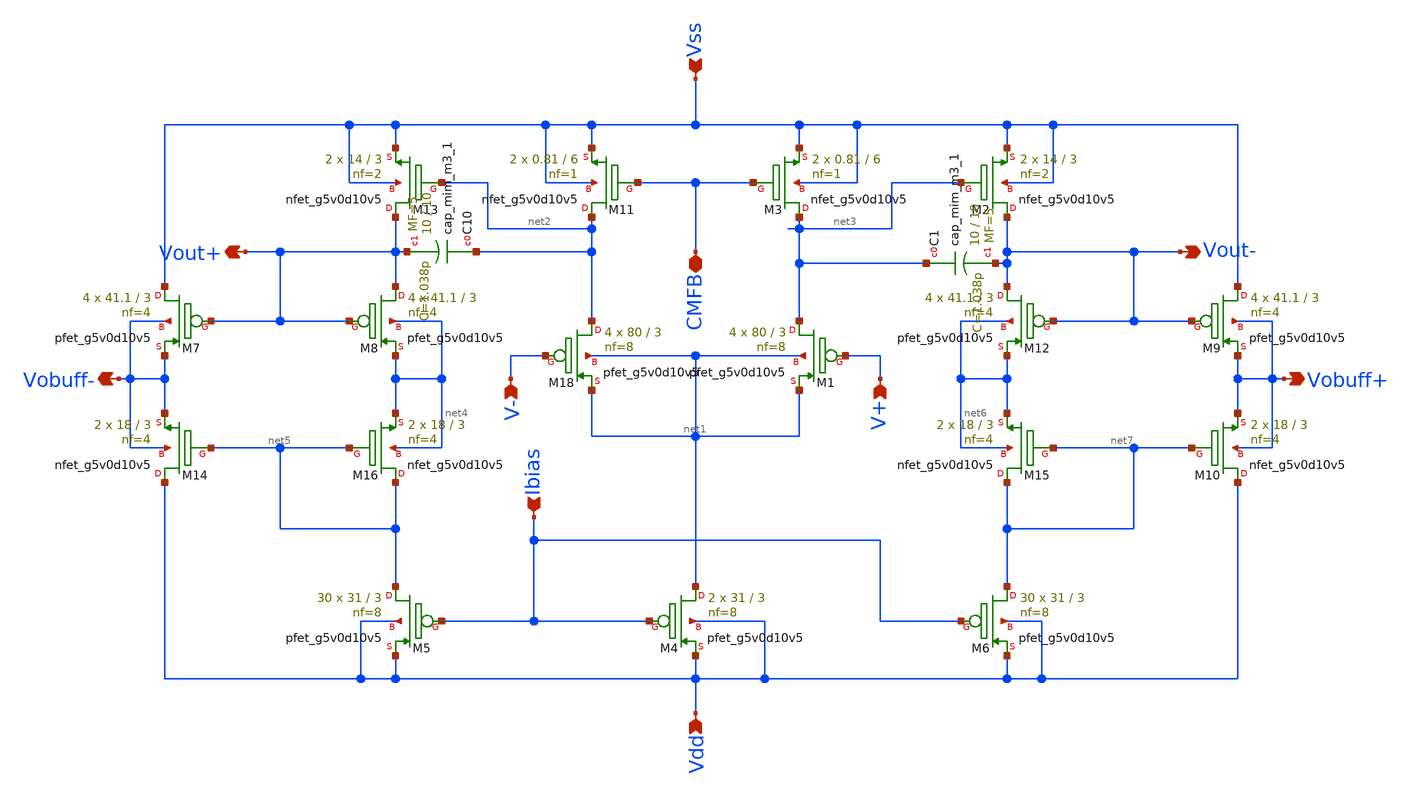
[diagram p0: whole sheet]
** sch_path: xschem/Diff_OP_AMP.sch
**.subckt Diff_OP_AMP Vout+ Vdd Vss V+ V- Vout- Ibias Vobuff- Vobuff+ CMFB
*.opin Vout+
*.ipin Vdd
*.ipin Vss
*.ipin V+
*.ipin V-
*.opin Vout-
*.ipin Ibias
*.opin Vobuff-
*.opin Vobuff+
*.iopin CMFB
XM4 net1 Ibias Vdd Vdd sky130_fd_pr__pfet_g5v0d10v5 L=3 W=31 nf=8 ad='int((8 + 1)/2) * 31 / 8 * 0.29'
+ as='int((8 + 2)/2) * 31 / 8 * 0.29' pd='2*int((8 + 1)/2) * (31 / 8 + 0.29)' ps='2*int((8 + 2)/2) * (31 / 8 + 0.29)'
+ nrd='0.29 / 31 ' nrs='0.29 / 31 ' sa=0 sb=0 sd=0 mult=2 m=2
XM18 net2 V- net1 net1 sky130_fd_pr__pfet_g5v0d10v5 L=3 W=80 nf=8 ad='int((8 + 1)/2) * 80 / 8 * 0.29'
+ as='int((8 + 2)/2) * 80 / 8 * 0.29' pd='2*int((8 + 1)/2) * (80 / 8 + 0.29)' ps='2*int((8 + 2)/2) * (80 / 8 + 0.29)'
+ nrd='0.29 / 80 ' nrs='0.29 / 80 ' sa=0 sb=0 sd=0 mult=4 m=4
XM1 net3 V+ net1 net1 sky130_fd_pr__pfet_g5v0d10v5 L=3 W=80 nf=8 ad='int((8 + 1)/2) * 80 / 8 * 0.29'
+ as='int((8 + 2)/2) * 80 / 8 * 0.29' pd='2*int((8 + 1)/2) * (80 / 8 + 0.29)' ps='2*int((8 + 2)/2) * (80 / 8 + 0.29)'
+ nrd='0.29 / 80 ' nrs='0.29 / 80 ' sa=0 sb=0 sd=0 mult=4 m=4
XM11 net2 CMFB Vss Vss sky130_fd_pr__nfet_g5v0d10v5 L=6 W=0.81 nf=1 ad='int((1 + 1)/2) * 0.81 / 1 * 0.29'
+ as='int((1 + 2)/2) * 0.81 / 1 * 0.29' pd='2*int((1 + 1)/2) * (0.81 / 1 + 0.29)' ps='2*int((1 + 2)/2) * (0.81 / 1 + 0.29)'
+ nrd='0.29 / 0.81 ' nrs='0.29 / 0.81 ' sa=0 sb=0 sd=0 mult=2 m=2
XM3 net3 CMFB Vss Vss sky130_fd_pr__nfet_g5v0d10v5 L=6 W=0.81 nf=1 ad='int((1 + 1)/2) * 0.81 / 1 * 0.29'
+ as='int((1 + 2)/2) * 0.81 / 1 * 0.29' pd='2*int((1 + 1)/2) * (0.81 / 1 + 0.29)' ps='2*int((1 + 2)/2) * (0.81 / 1 + 0.29)'
+ nrd='0.29 / 0.81 ' nrs='0.29 / 0.81 ' sa=0 sb=0 sd=0 mult=2 m=2
XM13 Vout+ net2 Vss Vss sky130_fd_pr__nfet_g5v0d10v5 L=3 W=14 nf=2 ad='int((2 + 1)/2) * 14 / 2 * 0.29'
+ as='int((2 + 2)/2) * 14 / 2 * 0.29' pd='2*int((2 + 1)/2) * (14 / 2 + 0.29)' ps='2*int((2 + 2)/2) * (14 / 2 + 0.29)'
+ nrd='0.29 / 14 ' nrs='0.29 / 14 ' sa=0 sb=0 sd=0 mult=2 m=2
XM2 Vout- net3 Vss Vss sky130_fd_pr__nfet_g5v0d10v5 L=3 W=14 nf=2 ad='int((2 + 1)/2) * 14 / 2 * 0.29'
+ as='int((2 + 2)/2) * 14 / 2 * 0.29' pd='2*int((2 + 1)/2) * (14 / 2 + 0.29)' ps='2*int((2 + 2)/2) * (14 / 2 + 0.29)'
+ nrd='0.29 / 14 ' nrs='0.29 / 14 ' sa=0 sb=0 sd=0 mult=2 m=2
XM5 net5 Ibias Vdd Vdd sky130_fd_pr__pfet_g5v0d10v5 L=3 W=31 nf=8 ad='int((8 + 1)/2) * 31 / 8 * 0.29'
+ as='int((8 + 2)/2) * 31 / 8 * 0.29' pd='2*int((8 + 1)/2) * (31 / 8 + 0.29)' ps='2*int((8 + 2)/2) * (31 / 8 + 0.29)'
+ nrd='0.29 / 31 ' nrs='0.29 / 31 ' sa=0 sb=0 sd=0 mult=30 m=30
XM6 net7 Ibias Vdd Vdd sky130_fd_pr__pfet_g5v0d10v5 L=3 W=31 nf=8 ad='int((8 + 1)/2) * 31 / 8 * 0.29'
+ as='int((8 + 2)/2) * 31 / 8 * 0.29' pd='2*int((8 + 1)/2) * (31 / 8 + 0.29)' ps='2*int((8 + 2)/2) * (31 / 8 + 0.29)'
+ nrd='0.29 / 31 ' nrs='0.29 / 31 ' sa=0 sb=0 sd=0 mult=30 m=30
XM8 Vout+ Vout+ net4 net4 sky130_fd_pr__pfet_g5v0d10v5 L=3 W=41.1 nf=4 ad='int((4 + 1)/2) * 41.1 / 4 * 0.29'
+ as='int((4 + 2)/2) * 41.1 / 4 * 0.29' pd='2*int((4 + 1)/2) * (41.1 / 4 + 0.29)' ps='2*int((4 + 2)/2) * (41.1 / 4 + 0.29)'
+ nrd='0.29 / 41.1 ' nrs='0.29 / 41.1 ' sa=0 sb=0 sd=0 mult=4 m=4
XM7 Vss Vout+ Vobuff- Vobuff- sky130_fd_pr__pfet_g5v0d10v5 L=3 W=41.1 nf=4 ad='int((4 + 1)/2) * 41.1 / 4 * 0.29'
+ as='int((4 + 2)/2) * 41.1 / 4 * 0.29' pd='2*int((4 + 1)/2) * (41.1 / 4 + 0.29)' ps='2*int((4 + 2)/2) * (41.1 / 4 + 0.29)'
+ nrd='0.29 / 41.1 ' nrs='0.29 / 41.1 ' sa=0 sb=0 sd=0 mult=4 m=4
XM9 Vss Vout- Vobuff+ Vobuff+ sky130_fd_pr__pfet_g5v0d10v5 L=3 W=41.1 nf=4 ad='int((4 + 1)/2) * 41.1 / 4 * 0.29'
+ as='int((4 + 2)/2) * 41.1 / 4 * 0.29' pd='2*int((4 + 1)/2) * (41.1 / 4 + 0.29)' ps='2*int((4 + 2)/2) * (41.1 / 4 + 0.29)'
+ nrd='0.29 / 41.1 ' nrs='0.29 / 41.1 ' sa=0 sb=0 sd=0 mult=4 m=4
XM12 Vout- Vout- net6 net6 sky130_fd_pr__pfet_g5v0d10v5 L=3 W=41.1 nf=4 ad='int((4 + 1)/2) * 41.1 / 4 * 0.29'
+ as='int((4 + 2)/2) * 41.1 / 4 * 0.29' pd='2*int((4 + 1)/2) * (41.1 / 4 + 0.29)' ps='2*int((4 + 2)/2) * (41.1 / 4 + 0.29)'
+ nrd='0.29 / 41.1 ' nrs='0.29 / 41.1 ' sa=0 sb=0 sd=0 mult=4 m=4
XM16 net5 net5 net4 net4 sky130_fd_pr__nfet_g5v0d10v5 L=3 W=18 nf=4 ad='int((4 + 1)/2) * 18 / 4 * 0.29'
+ as='int((4 + 2)/2) * 18 / 4 * 0.29' pd='2*int((4 + 1)/2) * (18 / 4 + 0.29)' ps='2*int((4 + 2)/2) * (18 / 4 + 0.29)'
+ nrd='0.29 / 18 ' nrs='0.29 / 18 ' sa=0 sb=0 sd=0 mult=2 m=2
XM14 Vdd net5 Vobuff- Vobuff- sky130_fd_pr__nfet_g5v0d10v5 L=3 W=18 nf=4 ad='int((4 + 1)/2) * 18 / 4 * 0.29'
+ as='int((4 + 2)/2) * 18 / 4 * 0.29' pd='2*int((4 + 1)/2) * (18 / 4 + 0.29)' ps='2*int((4 + 2)/2) * (18 / 4 + 0.29)'
+ nrd='0.29 / 18 ' nrs='0.29 / 18 ' sa=0 sb=0 sd=0 mult=2 m=2
XM10 Vdd net7 Vobuff+ Vobuff+ sky130_fd_pr__nfet_g5v0d10v5 L=3 W=18 nf=4 ad='int((4 + 1)/2) * 18 / 4 * 0.29'
+ as='int((4 + 2)/2) * 18 / 4 * 0.29' pd='2*int((4 + 1)/2) * (18 / 4 + 0.29)' ps='2*int((4 + 2)/2) * (18 / 4 + 0.29)'
+ nrd='0.29 / 18 ' nrs='0.29 / 18 ' sa=0 sb=0 sd=0 mult=2 m=2
XM15 net7 net7 net6 net6 sky130_fd_pr__nfet_g5v0d10v5 L=3 W=18 nf=4 ad='int((4 + 1)/2) * 18 / 4 * 0.29'
+ as='int((4 + 2)/2) * 18 / 4 * 0.29' pd='2*int((4 + 1)/2) * (18 / 4 + 0.29)' ps='2*int((4 + 2)/2) * (18 / 4 + 0.29)'
+ nrd='0.29 / 18 ' nrs='0.29 / 18 ' sa=0 sb=0 sd=0 mult=2 m=2
XC10 net2 Vout+ sky130_fd_pr__cap_mim_m3_1 W=10 L=10 MF=5 m=5
XC1 net3 Vout- sky130_fd_pr__cap_mim_m3_1 W=10 L=10 MF=5 m=5
**.ends
.end
